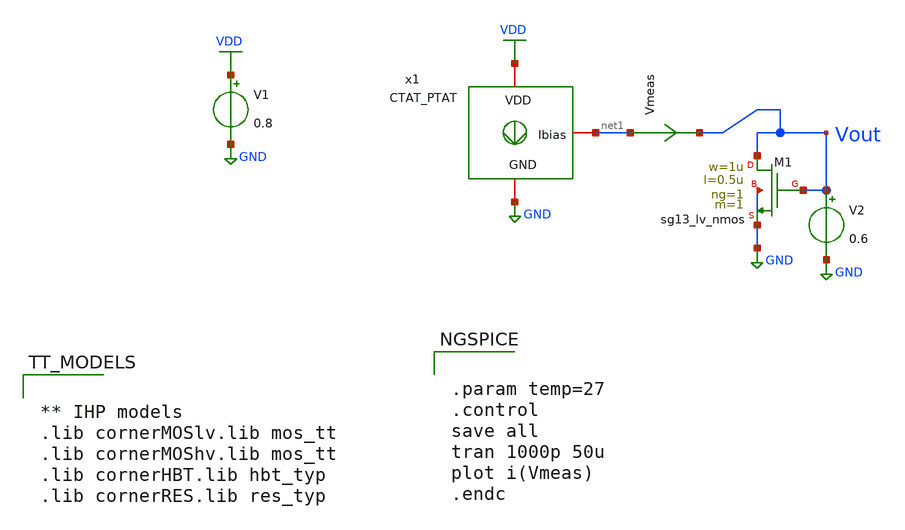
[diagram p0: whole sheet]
** sch_path: SSDOR_w_startup_1V_ihp/Ib_4u/CTAT_PTAT/tb_CTAT_PTAT.sch
**.subckt tb_CTAT_PTAT
V1 VDD GND 0.8
XM1 Vout Vout GND GND sg13_lv_nmos w=1u l=0.5u ng=1 m=1 mm_ok=1
x1 VDD net1 GND CTAT_PTAT
V2 Vout GND 0.6
Vmeas net1 Vout 0
.save i(vmeas)
**** begin user architecture code


** IHP models
.lib cornerMOSlv.lib mos_tt
.lib cornerMOShv.lib mos_tt
.lib cornerHBT.lib hbt_typ
.lib cornerRES.lib res_typ




.param temp=27
.control
save all
tran 1000p 50u
plot i(Vmeas)
.endc


**** end user architecture code
**.ends
.GLOBAL VDD
.GLOBAL GND
.end
